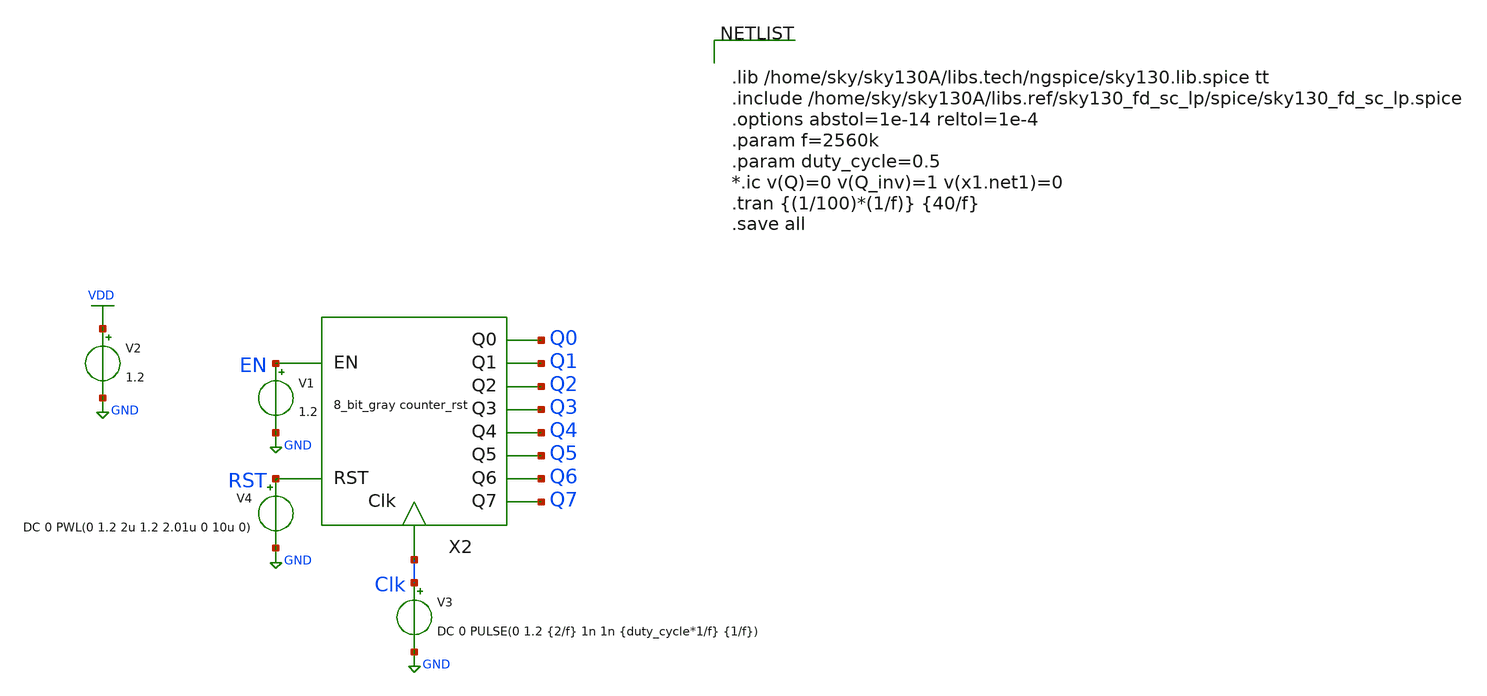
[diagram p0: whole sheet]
** sch_path: xschem/8_bit_gray_counter/8_bit_gray_counter_syn_rst_tb.sch
**.subckt 8_bit_gray_counter_syn_rst_tb
V3 Clk GND DC 0 PULSE(0 1.2 {2/f} 1n 1n {duty_cycle*1/f} {1/f})
V1 EN GND 1.2
V2 VDD GND 1.2
V4 RST GND DC 0 PWL(0 1.2 2u 1.2 2.01u 0 10u 0)
X2 EN RST Clk Q0 Q1 Q2 Q3 Q4 Q5 Q6 Q7 8_bit_gray_counter_syn_rst
**** begin user architecture code


.lib /home/sky/sky130A/libs.tech/ngspice/sky130.lib.spice tt
.include /home/sky/sky130A/libs.ref/sky130_fd_sc_lp/spice/sky130_fd_sc_lp.spice
.options abstol=1e-14 reltol=1e-4
.param f=2560k
.param duty_cycle=0.5
*.ic v(Q)=0 v(Q_inv)=1 v(x1.net1)=0
.tran {(1/100)*(1/f)} {40/f}
.save all


**** end user architecture code
**.ends

* expanding   symbol:  8_bit_gray_counter/8_bit_gray_counter_syn_rst.sym # of pins=11
** sym_path: xschem/8_bit_gray_counter/8_bit_gray_counter_syn_rst.sym
** sch_path: xschem/8_bit_gray_counter/8_bit_gray_counter_syn_rst.sch
.subckt 8_bit_gray_counter_syn_rst EN RST Clk Q0 Q1 Q2 Q3 Q4 Q5 Q6 Q7
*.ipin Clk
*.ipin EN
*.opin Q0
*.opin Q1
*.opin Q2
*.opin Q3
*.opin Q4
*.opin Q5
*.opin Q6
*.opin Q7
*.ipin RST
X10 net4 net5 net6 and_gate
X11 net6 net1 net7 and_gate
X12 net7 net2 net8 and_gate
X13 net8 net9 net10 and_gate
X14 net10 net11 net12 and_gate
X15 net12 net3 net13 and_gate
X16 net4 net5 Q0 exor_gate
X17 net5 net1 Q1 exor_gate
X18 net1 net2 Q2 exor_gate
X19 net2 net9 Q3 exor_gate
X20 net9 net11 Q4 exor_gate
X21 net11 net3 Q5 exor_gate
X22 net3 Q7 Q6 exor_gate
X30 net4 net5 net6 and_gate
X31 net6 net1 net7 and_gate
X32 net7 net2 net8 and_gate
X33 net8 net9 net10 and_gate
X34 net10 net11 net12 and_gate
X35 net12 net3 net13 and_gate
X36 net4 net5 Q0 exor_gate
X37 net5 net1 Q1 exor_gate
X38 net1 net2 Q2 exor_gate
X39 net2 net9 Q3 exor_gate
X40 net9 net11 Q4 exor_gate
X41 net11 net3 Q5 exor_gate
X42 net3 Q7 Q6 exor_gate
X1 EN net4 Clk RST t_ff_rst
X2 net4 net5 Clk RST t_ff_rst
X3 net6 net1 Clk RST t_ff_rst
X4 net7 net2 Clk RST t_ff_rst
X5 net8 net9 Clk RST t_ff_rst
X6 net10 net11 Clk RST t_ff_rst
X7 net12 net3 Clk RST t_ff_rst
X8 net13 Q7 Clk RST t_ff_rst
.ends


* expanding   symbol:  and_gate/and_gate.sym # of pins=3
** sym_path: xschem/and_gate/and_gate.sym
** sch_path: xschem/and_gate/and_gate.sch
.subckt and_gate A B out
*.ipin A
*.ipin B
*.opin out
XM1 net1 A net2 GND sky130_fd_pr__nfet_01v8 L=0.18 W=1 nf=1 ad='int((nf+1)/2) * W/nf * 0.29' as='int((nf+2)/2) * W/nf * 0.29'
+ pd='2*int((nf+1)/2) * (W/nf + 0.29)' ps='2*int((nf+2)/2) * (W/nf + 0.29)' nrd='0.29 / W' nrs='0.29 / W'
+ sa=0 sb=0 sd=0 mult=1 m=1
XM2 net1 A VDD VDD sky130_fd_pr__pfet_01v8 L=0.18 W=1 nf=1 ad='int((nf+1)/2) * W/nf * 0.29' as='int((nf+2)/2) * W/nf * 0.29'
+ pd='2*int((nf+1)/2) * (W/nf + 0.29)' ps='2*int((nf+2)/2) * (W/nf + 0.29)' nrd='0.29 / W' nrs='0.29 / W'
+ sa=0 sb=0 sd=0 mult=1 m=1
XM3 net1 B VDD VDD sky130_fd_pr__pfet_01v8 L=0.18 W=1 nf=1 ad='int((nf+1)/2) * W/nf * 0.29' as='int((nf+2)/2) * W/nf * 0.29'
+ pd='2*int((nf+1)/2) * (W/nf + 0.29)' ps='2*int((nf+2)/2) * (W/nf + 0.29)' nrd='0.29 / W' nrs='0.29 / W'
+ sa=0 sb=0 sd=0 mult=1 m=1
XM4 net2 B GND GND sky130_fd_pr__nfet_01v8 L=0.18 W=1 nf=1 ad='int((nf+1)/2) * W/nf * 0.29' as='int((nf+2)/2) * W/nf * 0.29'
+ pd='2*int((nf+1)/2) * (W/nf + 0.29)' ps='2*int((nf+2)/2) * (W/nf + 0.29)' nrd='0.29 / W' nrs='0.29 / W'
+ sa=0 sb=0 sd=0 mult=1 m=1
X1 net1 out inv Wpmos=3 Lpmos=0.18 Wnmos=1 Lnmos=0.18
.ends


* expanding   symbol:  exor_gate/exor_gate.sym # of pins=3
** sym_path: xschem/exor_gate/exor_gate.sym
** sch_path: xschem/exor_gate/exor_gate.sch
.subckt exor_gate A B out
*.ipin A
*.ipin B
*.opin out
XM4 out A net1 GND sky130_fd_pr__nfet_01v8 L=0.18 W=0.5 nf=1 ad='int((nf+1)/2) * W/nf * 0.29' as='int((nf+2)/2) * W/nf * 0.29'
+ pd='2*int((nf+1)/2) * (W/nf + 0.29)' ps='2*int((nf+2)/2) * (W/nf + 0.29)' nrd='0.29 / W' nrs='0.29 / W'
+ sa=0 sb=0 sd=0 mult=1 m=1
XM5 net3 B VDD VDD sky130_fd_pr__pfet_01v8 L=0.18 W=1 nf=1 ad='int((nf+1)/2) * W/nf * 0.29' as='int((nf+2)/2) * W/nf * 0.29'
+ pd='2*int((nf+1)/2) * (W/nf + 0.29)' ps='2*int((nf+2)/2) * (W/nf + 0.29)' nrd='0.29 / W' nrs='0.29 / W'
+ sa=0 sb=0 sd=0 mult=1 m=1
XM1 net1 B GND GND sky130_fd_pr__nfet_01v8 L=0.18 W=0.5 nf=1 ad='int((nf+1)/2) * W/nf * 0.29' as='int((nf+2)/2) * W/nf * 0.29'
+ pd='2*int((nf+1)/2) * (W/nf + 0.29)' ps='2*int((nf+2)/2) * (W/nf + 0.29)' nrd='0.29 / W' nrs='0.29 / W'
+ sa=0 sb=0 sd=0 mult=1 m=1
XM2 out net5 net3 VDD sky130_fd_pr__pfet_01v8 L=0.18 W=1 nf=1 ad='int((nf+1)/2) * W/nf * 0.29' as='int((nf+2)/2) * W/nf * 0.29'
+ pd='2*int((nf+1)/2) * (W/nf + 0.29)' ps='2*int((nf+2)/2) * (W/nf + 0.29)' nrd='0.29 / W' nrs='0.29 / W'
+ sa=0 sb=0 sd=0 mult=1 m=1
XM3 net4 net6 VDD VDD sky130_fd_pr__pfet_01v8 L=0.18 W=1 nf=1 ad='int((nf+1)/2) * W/nf * 0.29' as='int((nf+2)/2) * W/nf * 0.29'
+ pd='2*int((nf+1)/2) * (W/nf + 0.29)' ps='2*int((nf+2)/2) * (W/nf + 0.29)' nrd='0.29 / W' nrs='0.29 / W'
+ sa=0 sb=0 sd=0 mult=1 m=1
XM6 out A net4 VDD sky130_fd_pr__pfet_01v8 L=0.18 W=1 nf=1 ad='int((nf+1)/2) * W/nf * 0.29' as='int((nf+2)/2) * W/nf * 0.29'
+ pd='2*int((nf+1)/2) * (W/nf + 0.29)' ps='2*int((nf+2)/2) * (W/nf + 0.29)' nrd='0.29 / W' nrs='0.29 / W'
+ sa=0 sb=0 sd=0 mult=1 m=1
XM7 out net5 net2 GND sky130_fd_pr__nfet_01v8 L=0.18 W=0.5 nf=1 ad='int((nf+1)/2) * W/nf * 0.29' as='int((nf+2)/2) * W/nf * 0.29'
+ pd='2*int((nf+1)/2) * (W/nf + 0.29)' ps='2*int((nf+2)/2) * (W/nf + 0.29)' nrd='0.29 / W' nrs='0.29 / W'
+ sa=0 sb=0 sd=0 mult=1 m=1
XM8 net2 net6 GND GND sky130_fd_pr__nfet_01v8 L=0.18 W=0.5 nf=1 ad='int((nf+1)/2) * W/nf * 0.29' as='int((nf+2)/2) * W/nf * 0.29'
+ pd='2*int((nf+1)/2) * (W/nf + 0.29)' ps='2*int((nf+2)/2) * (W/nf + 0.29)' nrd='0.29 / W' nrs='0.29 / W'
+ sa=0 sb=0 sd=0 mult=1 m=1
X3 B net6 inv Wpmos=3 Lpmos=0.18 Wnmos=1 Lnmos=0.18
X2 A net5 inv Wpmos=3 Lpmos=0.18 Wnmos=1 Lnmos=0.18
.ends


* expanding   symbol:  T_flip_flop/t_ff_rst.sym # of pins=4
** sym_path: xschem/T_flip_flop/t_ff_rst.sym
** sch_path: xschem/T_flip_flop/t_ff_rst.sch
.subckt t_ff_rst T Q Clk RST
*.ipin T
*.ipin Clk
*.opin Q
*.ipin RST
X2 Q T net1 exor_gate
X3 net1 Q Clk RST d_ff_rst
.ends


* expanding   symbol:  inv/inv.sym # of pins=2
** sym_path: xschem/inv/inv.sym
** sch_path: xschem/inv/inv.sch
.subckt inv in out  Wpmos=3 Lpmos=0.18 Wnmos=1 Lnmos=0.18
*.ipin in
*.iopin out
XM1 out in GND GND sky130_fd_pr__nfet_01v8 L=Lnmos W=Wnmos nf=1 ad='int((nf+1)/2) * W/nf * 0.29' as='int((nf+2)/2) * W/nf * 0.29'
+ pd='2*int((nf+1)/2) * (W/nf + 0.29)' ps='2*int((nf+2)/2) * (W/nf + 0.29)' nrd='0.29 / W' nrs='0.29 / W'
+ sa=0 sb=0 sd=0 mult=1 m=1
XM2 out in VDD VDD sky130_fd_pr__pfet_01v8 L=Lpmos W=Wpmos nf=1 ad='int((nf+1)/2) * W/nf * 0.29' as='int((nf+2)/2) * W/nf * 0.29'
+ pd='2*int((nf+1)/2) * (W/nf + 0.29)' ps='2*int((nf+2)/2) * (W/nf + 0.29)' nrd='0.29 / W' nrs='0.29 / W'
+ sa=0 sb=0 sd=0 mult=1 m=1
.ends


* expanding   symbol:  D_flip_flop/d_ff_rst.sym # of pins=4
** sym_path: xschem/D_flip_flop/d_ff_rst.sym
** sch_path: xschem/D_flip_flop/d_ff_rst.sch
.subckt d_ff_rst D Q Clk RST
*.ipin D
*.ipin Clk
*.opin Q
*.ipin RST
X1 net1 net2 inv Wpmos=3 Lpmos=0.18 Wnmos=1 Lnmos=0.18
X2 net3 Q inv Wpmos=3 Lpmos=0.18 Wnmos=1 Lnmos=0.18
X3 net2 net4 inv Wpmos=3 Lpmos=0.18 Wnmos=1 Lnmos=0.18
X4 Q net5 inv Wpmos=3 Lpmos=0.18 Wnmos=1 Lnmos=0.18
X5 net7 net1 Clk net6 transmission_gate Wpmos=1 Lpmos=0.18 Wnmos=1 Lnmos=0.18
X6 net1 net4 net6 Clk transmission_gate Wpmos=1 Lpmos=0.18 Wnmos=1 Lnmos=0.18
X7 net3 net5 Clk net6 transmission_gate Wpmos=1 Lpmos=0.18 Wnmos=1 Lnmos=0.18
X8 net2 net3 net6 Clk transmission_gate Wpmos=1 Lpmos=0.18 Wnmos=1 Lnmos=0.18
X9 Clk net6 inv Wpmos=3 Lpmos=0.18 Wnmos=1 Lnmos=0.18
X10 net8 D net7 and_gate
X11 RST net8 inv Wpmos=3 Lpmos=0.18 Wnmos=1 Lnmos=0.18
.ends


* expanding   symbol:  transmission_gate/transmission_gate.sym # of pins=4
** sym_path: xschem/transmission_gate/transmission_gate.sym
** sch_path: xschem/transmission_gate/transmission_gate.sch
.subckt transmission_gate in out ctrl_ ctrl  Wpmos=1 Lpmos=0.18 Wnmos=1 Lnmos=0.18
*.iopin in
*.iopin out
*.ipin ctrl_
*.ipin ctrl
XM1 in ctrl out GND sky130_fd_pr__nfet_01v8 L=Lnmos W=Wnmos nf=1 ad='int((nf+1)/2) * W/nf * 0.29' as='int((nf+2)/2) * W/nf * 0.29'
+ pd='2*int((nf+1)/2) * (W/nf + 0.29)' ps='2*int((nf+2)/2) * (W/nf + 0.29)' nrd='0.29 / W' nrs='0.29 / W'
+ sa=0 sb=0 sd=0 mult=1 m=1
XM2 out ctrl_ in VDD sky130_fd_pr__pfet_01v8 L=Lpmos W=Wpmos nf=1 ad='int((nf+1)/2) * W/nf * 0.29' as='int((nf+2)/2) * W/nf * 0.29'
+ pd='2*int((nf+1)/2) * (W/nf + 0.29)' ps='2*int((nf+2)/2) * (W/nf + 0.29)' nrd='0.29 / W' nrs='0.29 / W'
+ sa=0 sb=0 sd=0 mult=1 m=1
.ends

.GLOBAL GND
.GLOBAL VDD
.end
